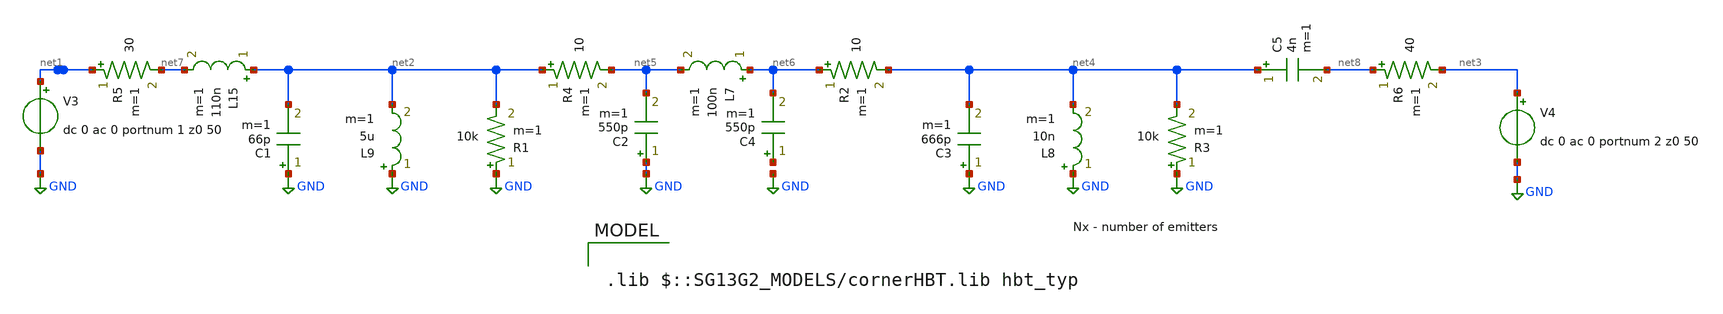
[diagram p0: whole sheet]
** sch_path: ihp-sg13g2/libs.tech/xschem/sg13g2_tests/sp_passives_test.sch
* Copyright 2023 IHP PDK Authors
**.subckt sp_passives_test
V4 net3 GND dc 0 ac 0 portnum 2 z0 50
V3 net1 GND dc 0 ac 0 portnum 1 z0 50
C1 GND net2 66p m=1
L9 GND net2 5u m=1
R1 GND net2 10k m=1
L7 net6 net5 100n m=1
R2 net6 net4 10 m=1
C2 GND net5 550p m=1
C3 GND net4 666p m=1
L8 GND net4 10n m=1
R3 GND net4 10k m=1
R4 net2 net5 10 m=1
C4 net9 net6 550p m=1
R5 net1 net7 30 m=1
L15 net2 net7 110n m=1
R6 net8 net3 40 m=1
C5 net4 net8 4n m=1
**** begin user architecture code

.lib $::SG13G2_MODELS/cornerHBT.lib hbt_typ



.param Rbase=50
.control
save all
sp dec 1000 9e4 1e11 1
let z11m = abs(z_1_1)
meas ac z11 FIND z11m AT=30e6
let phz=ph(z_1_1)
meas ac p11 FIND phz AT=30e6
let z22m = abs(z_2_2)
meas ac z22 FIND z22m AT=30e6
let phz22=ph(z_2_2)
meas ac p22 FIND phz22 AT=30e6


let s11m = abs(s_1_1)
meas ac s11 FIND s11m at=1e9
let phs11=ph(s_1_1)
meas ac ps11 FIND phs11 at=1e9

let s22m = abs(s_2_2)
meas ac s22 FIND s22m at=1e9
let phs22=ph(s_2_2)
meas ac ps22 FIND phs22 at=1e9

set color0 = white
set color1 = red
set color2 = blue
set xbrushwidth=5

*plot s_1_1 smithgrid
*plot z_1_1 smith

*meas ac s21_max max s_2_1 from=9e8 to=5.1e9
write sp_hbt_13g2_lna.raw
*reset
*save all
*noise V(Vc) v3 lin 10k 9e8 1.1e9
*print inoise_total onoise_total
*setplot noise1
*write noise_hbt_13g2_lna.raw all
.endc


**** end user architecture code
**.ends
.GLOBAL GND
.end
